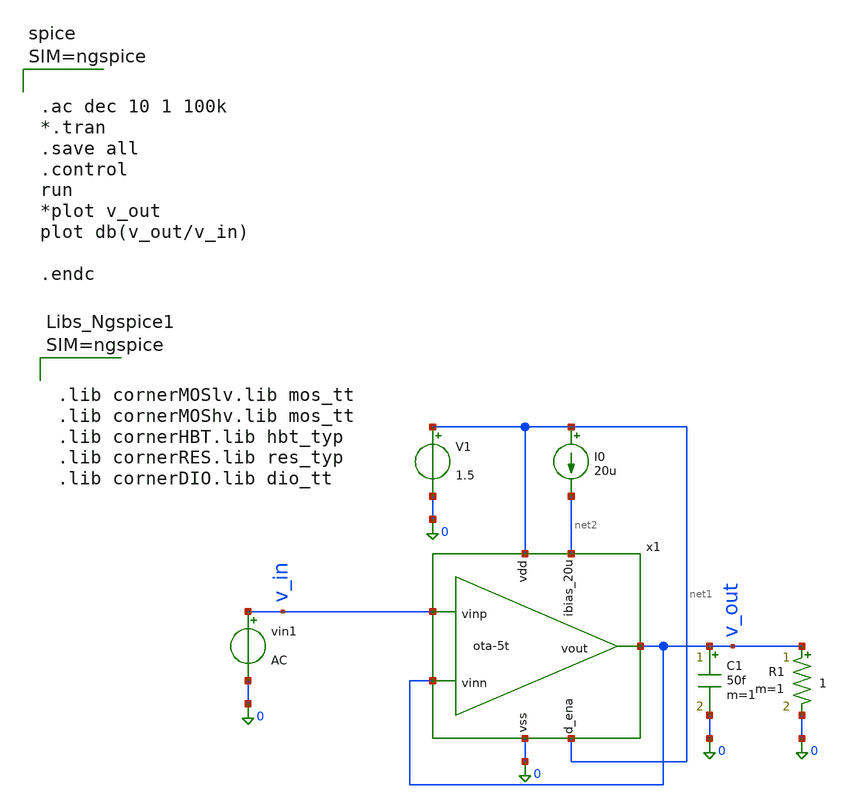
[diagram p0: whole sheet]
** sch_path: 004_Real_Circuits/5T_ota_tb.sch
* 004_Real_Circuits/ota-5t.sch:
* (c) 2024-2025 Harald Pretl, Apache-2.0 license
**.subckt 5T_ota_tb
x1 net1 v_out v_in v_out net2 net1 0 ota-5t
V1 net1 0 1.5
I0 net1 net2 20u
vin1 v_in 0 AC
R1 v_out 0 1 m=1
C1 v_out 0 50f m=1
**** begin user architecture code



.lib cornerMOSlv.lib mos_tt
.lib cornerMOShv.lib mos_tt
.lib cornerHBT.lib hbt_typ
.lib cornerRES.lib res_typ
.lib cornerDIO.lib dio_tt






.ac dec 10 1 100k
*.tran
.save all
.control
run
*plot v_out
plot db(v_out/v_in)

.endc



**** end user architecture code
**.ends

* expanding   symbol:  /foss/designs/004_Real_Circuits/ota-5t.sym # of pins=7
** sym_path: /foss/designs/004_Real_Circuits/ota-5t.sym
** sch_path: /foss/designs/004_Real_Circuits/ota-5t.sch
.subckt ota-5t vdd vout vinp vinn ibias_20u d_ena vss
*.ipin ibias_20u
*.iopin vdd
*.iopin vss
*.ipin vinp
*.ipin vinn
*.opin vout
*.ipin d_ena
XM5 tail gate_n vss vss sg13_lv_nmos w=1.5u l=5u ng=1 m=1 mm_ok=1
XM4 vout gate_p vdd vdd sg13_lv_pmos w=3.5u l=5u ng=1 m=1 mm_ok=1
XM1 gate_p vinp tail vss sg13_lv_nmos w=2u l=5u ng=1 m=1 mm_ok=1
XM2 vout vinn tail vss sg13_lv_nmos w=2u l=5u ng=1 m=1 mm_ok=1
XM3 gate_p gate_p vdd vdd sg13_lv_pmos w=3.5u l=5u ng=1 m=1 mm_ok=1
XM6 ibias_20u gate_n vss vss sg13_lv_nmos w=7.5u l=5u ng=5 m=1 mm_ok=1
XM9 gate_n ena_n vss vss sg13_lv_nmos w=0.5u l=0.13u ng=1 m=1 mm_ok=1
XM11 gate_p ena vdd vdd sg13_lv_pmos w=1.5u l=0.13u ng=1 m=1 mm_ok=1
XM7 ena ena_n vss vss sg13_lv_nmos w=0.5u l=0.13u ng=1 m=1 mm_ok=1
XM8 ena ena_n vdd vdd sg13_lv_pmos w=1.5u l=0.13u ng=1 m=1 mm_ok=1
XM10 ibias_20u ena gate_n vss sg13_lv_nmos w=0.5u l=0.13u ng=1 m=1 mm_ok=1
XM12 ena_n d_ena vss vss sg13_lv_nmos w=0.5u l=0.13u ng=1 m=1 mm_ok=1
XM13 ena_n d_ena vdd vdd sg13_lv_pmos w=1.5u l=0.13u ng=1 m=1 mm_ok=1
.ends

.end
